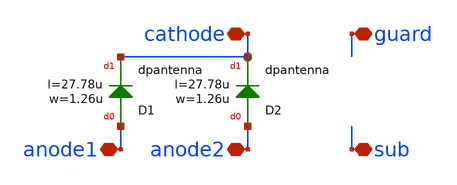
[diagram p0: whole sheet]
** sch_path: ihp-sg13cmos5l/libs.tech/xschem/hm_stdcells/sg13cmos5l_DCPDiode.sch
**.subckt sg13cmos5l_DCPDiode anode2 cathode guard anode1 sub
*.iopin anode2
*.iopin cathode
*.iopin guard
*.iopin anode1
*.iopin sub
XD1 anode1 cathode dpantenna l=27.78u w=1.26u
XD2 anode2 cathode dpantenna l=27.78u w=1.26u
**.ends
.end
